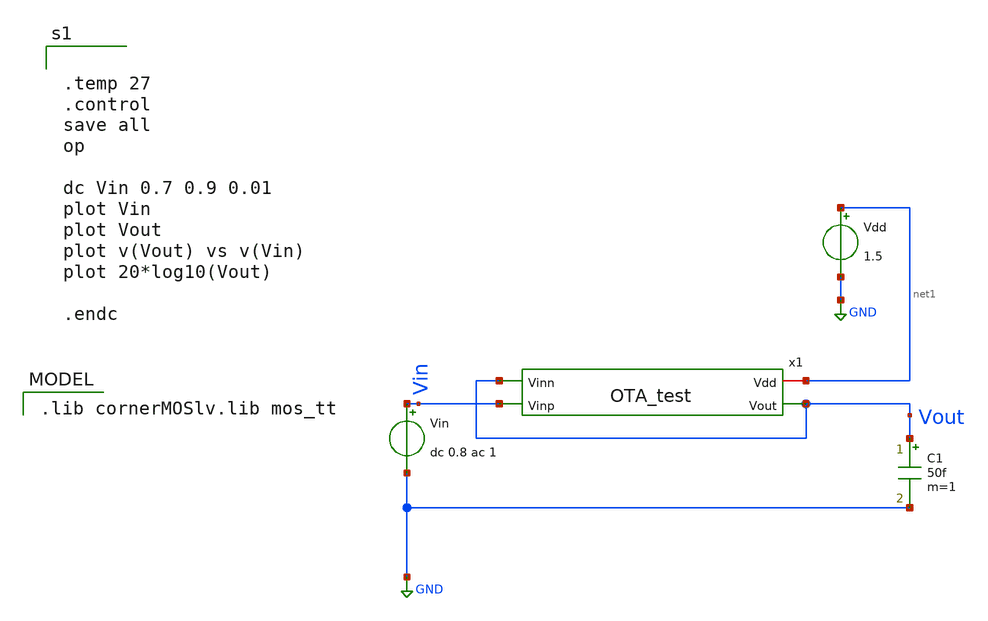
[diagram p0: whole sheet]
** sch_path: Xschem/Voltage_buffer.sch
**.subckt Voltage_buffer
Vin Vin GND dc 0.8 ac 1
Vdd net1 GND 1.5
C1 Vout GND 50f m=1
x1 net1 Vout Vout Vin OTA_test
**** begin user architecture code


.temp 27
.control
save all
op

dc Vin 0.7 0.9 0.01
plot Vin
plot Vout
plot v(Vout) vs v(Vin)
plot 20*log10(Vout)

.endc


 .lib cornerMOSlv.lib mos_tt

**** end user architecture code
**.ends

* expanding   symbol:  OTA_test.sym # of pins=4
** sym_path: Xschem/OTA_test.sym
** sch_path: Xschem/OTA_test.sch
.subckt OTA_test Vdd Vout Vinn Vinp
*.opin Vout
*.iopin Vdd
*.ipin Vinp
*.ipin Vinn
I_basis Vdd net3 20u
XM1 net1 Vinp net2 GND sg13_lv_nmos w=2u l=5u ng=1 m=1 mm_ok=1
XM5 net2 net3 GND GND sg13_lv_nmos w=0.5u l=5u ng=1 m=1 mm_ok=1
XM6 net3 net3 GND GND sg13_lv_nmos w=2.5u l=5u ng=5 m=1 mm_ok=1
XM4 Vout net1 Vdd Vdd sg13_lv_pmos w=1.5u l=5u ng=1 m=1 mm_ok=1
XM3 net1 net1 Vdd Vdd sg13_lv_pmos w=1.5u l=5u ng=1 m=1 mm_ok=1
XM2 Vout Vinn net2 GND sg13_lv_nmos w=2u l=5u ng=1 m=1 mm_ok=1
.ends

.GLOBAL GND
.end
